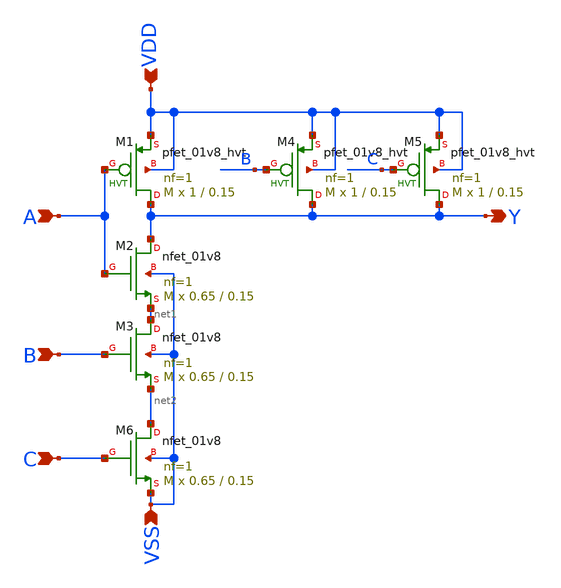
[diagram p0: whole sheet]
** sch_path: designs/nand3.sch
**.subckt nand3 A B Y C VDD VSS
*.ipin A
*.ipin B
*.opin Y
*.ipin C
*.ipin VDD
*.ipin VSS
XM2 Y A net1 VSS sky130_fd_pr__nfet_01v8 L=0.15 W=0.65 nf=1 ad='int((nf+1)/2) * W/nf * 0.29' as='int((nf+2)/2) * W/nf * 0.29'
+ pd='2*int((nf+1)/2) * (W/nf + 0.29)' ps='2*int((nf+2)/2) * (W/nf + 0.29)' nrd='0.29 / W' nrs='0.29 / W'
+ sa=0 sb=0 sd=0 mult=M m=M
XM1 Y A VDD VDD sky130_fd_pr__pfet_01v8_hvt L=0.15 W=1 nf=1 ad='int((nf+1)/2) * W/nf * 0.29' as='int((nf+2)/2) * W/nf * 0.29'
+ pd='2*int((nf+1)/2) * (W/nf + 0.29)' ps='2*int((nf+2)/2) * (W/nf + 0.29)' nrd='0.29 / W' nrs='0.29 / W'
+ sa=0 sb=0 sd=0 mult=M m=M
XM3 net1 B net2 VSS sky130_fd_pr__nfet_01v8 L=0.15 W=0.65 nf=1 ad='int((nf+1)/2) * W/nf * 0.29' as='int((nf+2)/2) * W/nf * 0.29'
+ pd='2*int((nf+1)/2) * (W/nf + 0.29)' ps='2*int((nf+2)/2) * (W/nf + 0.29)' nrd='0.29 / W' nrs='0.29 / W'
+ sa=0 sb=0 sd=0 mult=M m=M
XM4 Y B VDD VDD sky130_fd_pr__pfet_01v8_hvt L=0.15 W=1 nf=1 ad='int((nf+1)/2) * W/nf * 0.29' as='int((nf+2)/2) * W/nf * 0.29'
+ pd='2*int((nf+1)/2) * (W/nf + 0.29)' ps='2*int((nf+2)/2) * (W/nf + 0.29)' nrd='0.29 / W' nrs='0.29 / W'
+ sa=0 sb=0 sd=0 mult=M m=M
XM5 Y C VDD VDD sky130_fd_pr__pfet_01v8_hvt L=0.15 W=1 nf=1 ad='int((nf+1)/2) * W/nf * 0.29' as='int((nf+2)/2) * W/nf * 0.29'
+ pd='2*int((nf+1)/2) * (W/nf + 0.29)' ps='2*int((nf+2)/2) * (W/nf + 0.29)' nrd='0.29 / W' nrs='0.29 / W'
+ sa=0 sb=0 sd=0 mult=M m=M
XM6 net2 C VSS VSS sky130_fd_pr__nfet_01v8 L=0.15 W=0.65 nf=1 ad='int((nf+1)/2) * W/nf * 0.29' as='int((nf+2)/2) * W/nf * 0.29'
+ pd='2*int((nf+1)/2) * (W/nf + 0.29)' ps='2*int((nf+2)/2) * (W/nf + 0.29)' nrd='0.29 / W' nrs='0.29 / W'
+ sa=0 sb=0 sd=0 mult=M m=M
**.ends
.end
